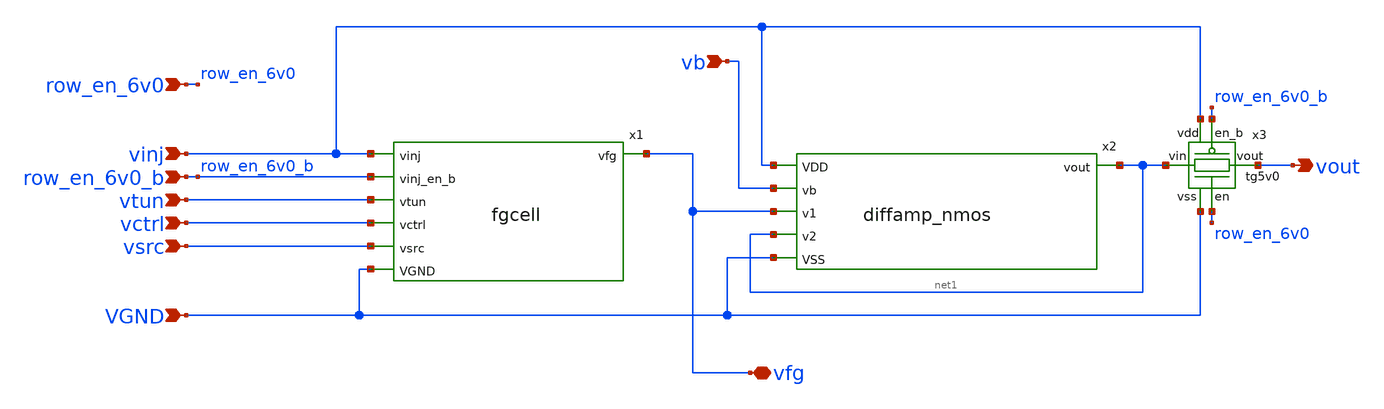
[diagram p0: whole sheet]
** sch_path: xschem/fgcell_amp.sch
**.subckt fgcell_amp vinj row_en_6v0_b vtun vctrl vsrc vb VGND vout vfg row_en_6v0
*.ipin vinj
*.ipin row_en_6v0_b
*.ipin vtun
*.ipin vctrl
*.ipin vsrc
*.ipin vb
*.ipin VGND
*.opin vout
*.iopin vfg
*.ipin row_en_6v0
x1 vinj row_en_6v0_b vtun vctrl vsrc VGND vfg fgcell
x2 vfg net1 VGND vinj vb net1 diffamp_nmos
x3 net1 vout row_en_6v0 row_en_6v0_b vinj VGND tg5v0
**.ends

* expanding   symbol:  fgcell.sym # of pins=7
** sym_path: xschem/fgcell.sym
** sch_path: xschem/fgcell.sch
.subckt fgcell vinj vinj_en_b vtun vctrl vsrc VGND vfg
*.ipin vinj
*.ipin vinj_en_b
*.ipin vtun
*.ipin vctrl
*.ipin vsrc
*.ipin VGND
*.opin vfg
XM1 vsrc vfg net1 vinj sky130_fd_pr__pfet_g5v0d10v5 L=0.5 W=1 nf=1 ad='int((nf+1)/2) * W/nf * 0.29' as='int((nf+2)/2) * W/nf * 0.29'
+ pd='2*int((nf+1)/2) * (W/nf + 0.29)' ps='2*int((nf+2)/2) * (W/nf + 0.29)' nrd='0.29 / W' nrs='0.29 / W'
+ sa=0 sb=0 sd=0 mult=1 m=1
XM2 net1 vinj_en_b vinj vinj sky130_fd_pr__pfet_g5v0d10v5 L=0.5 W=1 nf=1 ad='int((nf+1)/2) * W/nf * 0.29'
+ as='int((nf+2)/2) * W/nf * 0.29' pd='2*int((nf+1)/2) * (W/nf + 0.29)' ps='2*int((nf+2)/2) * (W/nf + 0.29)'
+ nrd='0.29 / W' nrs='0.29 / W' sa=0 sb=0 sd=0 mult=1 m=1
XC1 vfg vtun VGND sky130_fd_pr__cap_var_hvt W=1 L=0.5 VM=1 m=1
XM3 vctrl vfg vctrl vctrl sky130_fd_pr__pfet_g5v0d10v5 L=0.5 W=1 nf=1 ad='int((nf+1)/2) * W/nf * 0.29'
+ as='int((nf+2)/2) * W/nf * 0.29' pd='2*int((nf+1)/2) * (W/nf + 0.29)' ps='2*int((nf+2)/2) * (W/nf + 0.29)'
+ nrd='0.29 / W' nrs='0.29 / W' sa=0 sb=0 sd=0 mult=1 m=1
.ends


* expanding   symbol:  diffamp_nmos.sym # of pins=6
** sym_path: xschem/diffamp_nmos.sym
** sch_path: xschem/diffamp_nmos.sch
.subckt diffamp_nmos v1 v2 VSS VDD vb vout
*.ipin v1
*.ipin v2
*.ipin vb
*.opin vout
*.ipin VDD
*.ipin VSS
XM7 int2 int3 VDD VDD sky130_fd_pr__pfet_g5v0d10v5 L=1 W=1.5 nf=1 ad='int((nf+1)/2) * W/nf * 0.29' as='int((nf+2)/2) * W/nf * 0.29'
+ pd='2*int((nf+1)/2) * (W/nf + 0.29)' ps='2*int((nf+2)/2) * (W/nf + 0.29)' nrd='0.29 / W' nrs='0.29 / W'
+ sa=0 sb=0 sd=0 mult=1 m=1
XM8 int2 int2 VSS VSS sky130_fd_pr__nfet_g5v0d10v5 L=1 W=1.5 nf=1 ad='int((nf+1)/2) * W/nf * 0.29' as='int((nf+2)/2) * W/nf * 0.29'
+ pd='2*int((nf+1)/2) * (W/nf + 0.29)' ps='2*int((nf+2)/2) * (W/nf + 0.29)' nrd='0.29 / W' nrs='0.29 / W'
+ sa=0 sb=0 sd=0 mult=1 m=1
XM9 vout int2 VSS VSS sky130_fd_pr__nfet_g5v0d10v5 L=1 W=1.5 nf=1 ad='int((nf+1)/2) * W/nf * 0.29' as='int((nf+2)/2) * W/nf * 0.29'
+ pd='2*int((nf+1)/2) * (W/nf + 0.29)' ps='2*int((nf+2)/2) * (W/nf + 0.29)' nrd='0.29 / W' nrs='0.29 / W'
+ sa=0 sb=0 sd=0 mult=1 m=1
XM1 int4 v1 int1 VSS sky130_fd_pr__nfet_g5v0d10v5 L=1 W=1.5 nf=1 ad='int((nf+1)/2) * W/nf * 0.29' as='int((nf+2)/2) * W/nf * 0.29'
+ pd='2*int((nf+1)/2) * (W/nf + 0.29)' ps='2*int((nf+2)/2) * (W/nf + 0.29)' nrd='0.29 / W' nrs='0.29 / W'
+ sa=0 sb=0 sd=0 mult=1 m=1
XM2 int3 v2 int1 VSS sky130_fd_pr__nfet_g5v0d10v5 L=1 W=1.5 nf=1 ad='int((nf+1)/2) * W/nf * 0.29' as='int((nf+2)/2) * W/nf * 0.29'
+ pd='2*int((nf+1)/2) * (W/nf + 0.29)' ps='2*int((nf+2)/2) * (W/nf + 0.29)' nrd='0.29 / W' nrs='0.29 / W'
+ sa=0 sb=0 sd=0 mult=1 m=1
XM6 int3 int3 VDD VDD sky130_fd_pr__pfet_g5v0d10v5 L=1 W=1.5 nf=1 ad='int((nf+1)/2) * W/nf * 0.29' as='int((nf+2)/2) * W/nf * 0.29'
+ pd='2*int((nf+1)/2) * (W/nf + 0.29)' ps='2*int((nf+2)/2) * (W/nf + 0.29)' nrd='0.29 / W' nrs='0.29 / W'
+ sa=0 sb=0 sd=0 mult=1 m=1
XM5 vout int4 VDD VDD sky130_fd_pr__pfet_g5v0d10v5 L=1 W=1.5 nf=1 ad='int((nf+1)/2) * W/nf * 0.29' as='int((nf+2)/2) * W/nf * 0.29'
+ pd='2*int((nf+1)/2) * (W/nf + 0.29)' ps='2*int((nf+2)/2) * (W/nf + 0.29)' nrd='0.29 / W' nrs='0.29 / W'
+ sa=0 sb=0 sd=0 mult=1 m=1
XM3a int1 vb int5 VSS sky130_fd_pr__nfet_g5v0d10v5 L=1 W=1.5 nf=1 ad='int((nf+1)/2) * W/nf * 0.29' as='int((nf+2)/2) * W/nf * 0.29'
+ pd='2*int((nf+1)/2) * (W/nf + 0.29)' ps='2*int((nf+2)/2) * (W/nf + 0.29)' nrd='0.29 / W' nrs='0.29 / W'
+ sa=0 sb=0 sd=0 mult=1 m=1
XM3b int5 vb VSS VSS sky130_fd_pr__nfet_g5v0d10v5 L=1 W=1.5 nf=1 ad='int((nf+1)/2) * W/nf * 0.29' as='int((nf+2)/2) * W/nf * 0.29'
+ pd='2*int((nf+1)/2) * (W/nf + 0.29)' ps='2*int((nf+2)/2) * (W/nf + 0.29)' nrd='0.29 / W' nrs='0.29 / W'
+ sa=0 sb=0 sd=0 mult=1 m=1
XM4 int4 int4 VDD VDD sky130_fd_pr__pfet_g5v0d10v5 L=1 W=1.5 nf=1 ad='int((nf+1)/2) * W/nf * 0.29' as='int((nf+2)/2) * W/nf * 0.29'
+ pd='2*int((nf+1)/2) * (W/nf + 0.29)' ps='2*int((nf+2)/2) * (W/nf + 0.29)' nrd='0.29 / W' nrs='0.29 / W'
+ sa=0 sb=0 sd=0 mult=1 m=1
.ends


* expanding   symbol:  tg5v0.sym # of pins=6
** sym_path: xschem/tg5v0.sym
** sch_path: xschem/tg5v0.sch
.subckt tg5v0 vin vout en en_b vdd vss
*.ipin vin
*.opin vout
*.ipin en
*.ipin en_b
*.ipin vdd
*.ipin vss
XM1 vout en vin vss sky130_fd_pr__nfet_g5v0d10v5 L=0.5 W=4 nf=8 ad='int((nf+1)/2) * W/nf * 0.29' as='int((nf+2)/2) * W/nf * 0.29'
+ pd='2*int((nf+1)/2) * (W/nf + 0.29)' ps='2*int((nf+2)/2) * (W/nf + 0.29)' nrd='0.29 / W' nrs='0.29 / W'
+ sa=0 sb=0 sd=0 mult=1 m=1
XM2 vout en_b vin vdd sky130_fd_pr__pfet_g5v0d10v5 L=0.5 W=4 nf=8 ad='int((nf+1)/2) * W/nf * 0.29' as='int((nf+2)/2) * W/nf * 0.29'
+ pd='2*int((nf+1)/2) * (W/nf + 0.29)' ps='2*int((nf+2)/2) * (W/nf + 0.29)' nrd='0.29 / W' nrs='0.29 / W'
+ sa=0 sb=0 sd=0 mult=1 m=1
.ends

.end
